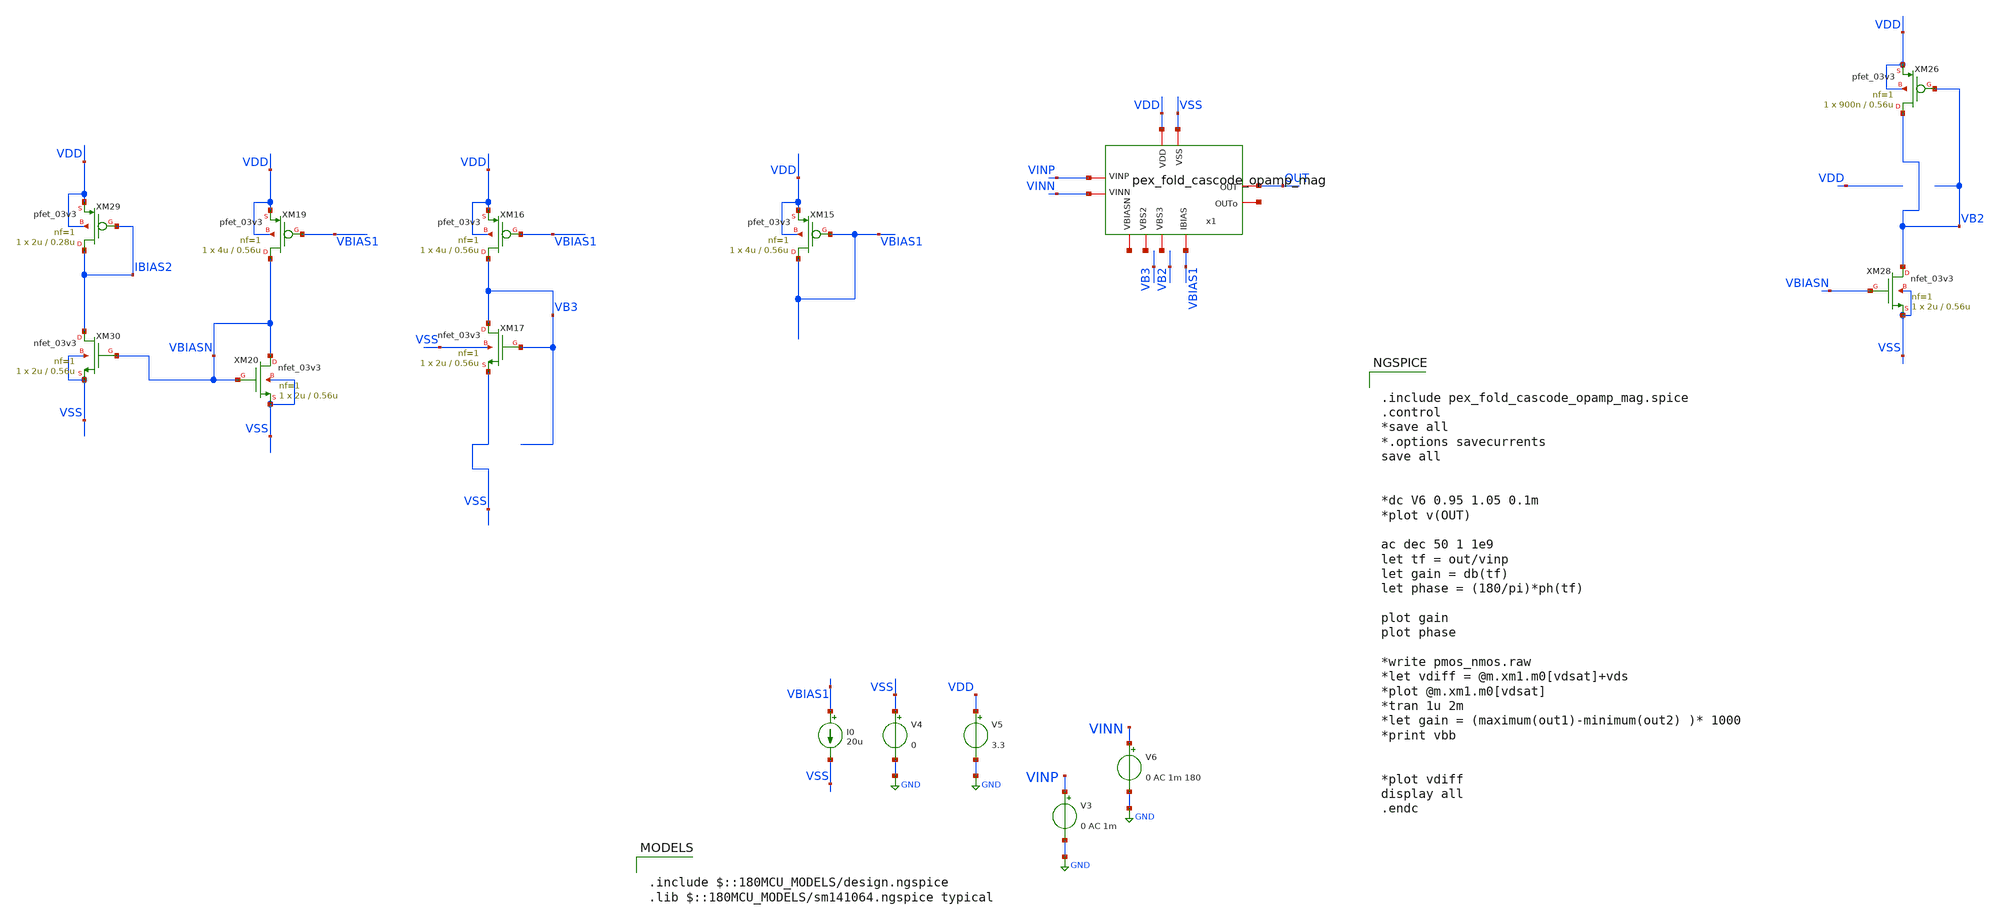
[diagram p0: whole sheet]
** sch_path: SCOP_INPUT_AND_MUX_PAKISTAN_03/Xschem/Folded_single/opamp_new_pex.sch
**.subckt opamp_new_pex
V3 VINP GND 0 AC 1m
V4 VSS GND 0
V5 VDD GND 3.3
V6 VINN GND 0 AC 1m 180
I0 VBIAS1 VSS 20u
XM15 VBIAS1 VBIAS1 VDD VDD pfet_03v3 L=0.56u W=4u nf=1 ad='int((nf+1)/2) * W/nf * 0.18u' as='int((nf+2)/2) * W/nf * 0.18u'
+ pd='2*int((nf+1)/2) * (W/nf + 0.18u)' ps='2*int((nf+2)/2) * (W/nf + 0.18u)' nrd='0.18u / W' nrs='0.18u / W'
+ sa=0 sb=0 sd=0 m=1
XM16 VB3 VBIAS1 VDD VDD pfet_03v3 L=0.56u W=4u nf=1 ad='int((nf+1)/2) * W/nf * 0.18u' as='int((nf+2)/2) * W/nf * 0.18u'
+ pd='2*int((nf+1)/2) * (W/nf + 0.18u)' ps='2*int((nf+2)/2) * (W/nf + 0.18u)' nrd='0.18u / W' nrs='0.18u / W'
+ sa=0 sb=0 sd=0 m=1
XM17 VB3 VB3 VSS VSS nfet_03v3 L=0.56u W=2u nf=1 ad='int((nf+1)/2) * W/nf * 0.18u' as='int((nf+2)/2) * W/nf * 0.18u'
+ pd='2*int((nf+1)/2) * (W/nf + 0.18u)' ps='2*int((nf+2)/2) * (W/nf + 0.18u)' nrd='0.18u / W' nrs='0.18u / W'
+ sa=0 sb=0 sd=0 m=1
XM19 VBIASN VBIAS1 VDD VDD pfet_03v3 L=0.56u W=4u nf=1 ad='int((nf+1)/2) * W/nf * 0.18u' as='int((nf+2)/2) * W/nf * 0.18u'
+ pd='2*int((nf+1)/2) * (W/nf + 0.18u)' ps='2*int((nf+2)/2) * (W/nf + 0.18u)' nrd='0.18u / W' nrs='0.18u / W'
+ sa=0 sb=0 sd=0 m=1
XM20 VBIASN VBIASN VSS VSS nfet_03v3 L=0.56u W=2u nf=1 ad='int((nf+1)/2) * W/nf * 0.18u' as='int((nf+2)/2) * W/nf * 0.18u'
+ pd='2*int((nf+1)/2) * (W/nf + 0.18u)' ps='2*int((nf+2)/2) * (W/nf + 0.18u)' nrd='0.18u / W' nrs='0.18u / W'
+ sa=0 sb=0 sd=0 m=1
XM26 VB2 VB2 VDD VDD pfet_03v3 L=0.56u W=900n nf=1 ad='int((nf+1)/2) * W/nf * 0.18u' as='int((nf+2)/2) * W/nf * 0.18u'
+ pd='2*int((nf+1)/2) * (W/nf + 0.18u)' ps='2*int((nf+2)/2) * (W/nf + 0.18u)' nrd='0.18u / W' nrs='0.18u / W'
+ sa=0 sb=0 sd=0 m=1
XM28 VB2 VBIASN VSS VSS nfet_03v3 L=0.56u W=2u nf=1 ad='int((nf+1)/2) * W/nf * 0.18u' as='int((nf+2)/2) * W/nf * 0.18u'
+ pd='2*int((nf+1)/2) * (W/nf + 0.18u)' ps='2*int((nf+2)/2) * (W/nf + 0.18u)' nrd='0.18u / W' nrs='0.18u / W'
+ sa=0 sb=0 sd=0 m=1
XM29 IBIAS2 IBIAS2 VDD VDD pfet_03v3 L=0.28u W=2u nf=1 ad='int((nf+1)/2) * W/nf * 0.18u' as='int((nf+2)/2) * W/nf * 0.18u'
+ pd='2*int((nf+1)/2) * (W/nf + 0.18u)' ps='2*int((nf+2)/2) * (W/nf + 0.18u)' nrd='0.18u / W' nrs='0.18u / W'
+ sa=0 sb=0 sd=0 m=1
XM30 IBIAS2 VBIASN VSS VSS nfet_03v3 L=0.56u W=2u nf=1 ad='int((nf+1)/2) * W/nf * 0.18u' as='int((nf+2)/2) * W/nf * 0.18u'
+ pd='2*int((nf+1)/2) * (W/nf + 0.18u)' ps='2*int((nf+2)/2) * (W/nf + 0.18u)' nrd='0.18u / W' nrs='0.18u / W'
+ sa=0 sb=0 sd=0 m=1
x1 OUT VDD VSS VINN VINP VBIAS1 net1 net2 net3 net4 pex_fold_cascode_opamp_mag
**** begin user architecture code

.include $::180MCU_MODELS/design.ngspice
.lib $::180MCU_MODELS/sm141064.ngspice typical



.include pex_fold_cascode_opamp_mag.spice
.control
*save all
*.options savecurrents
save all


*dc V6 0.95 1.05 0.1m
*plot v(OUT)

ac dec 50 1 1e9
let tf = out/vinp
let gain = db(tf)
let phase = (180/pi)*ph(tf)

plot gain
plot phase

*write pmos_nmos.raw
*let vdiff = @m.xm1.m0[vdsat]+vds
*plot @m.xm1.m0[vdsat]
*tran 1u 2m
*let gain = (maximum(out1)-minimum(out2) )* 1000
*print vbb


*plot vdiff
display all
.endc


**** end user architecture code
**.ends
.GLOBAL GND
.end
